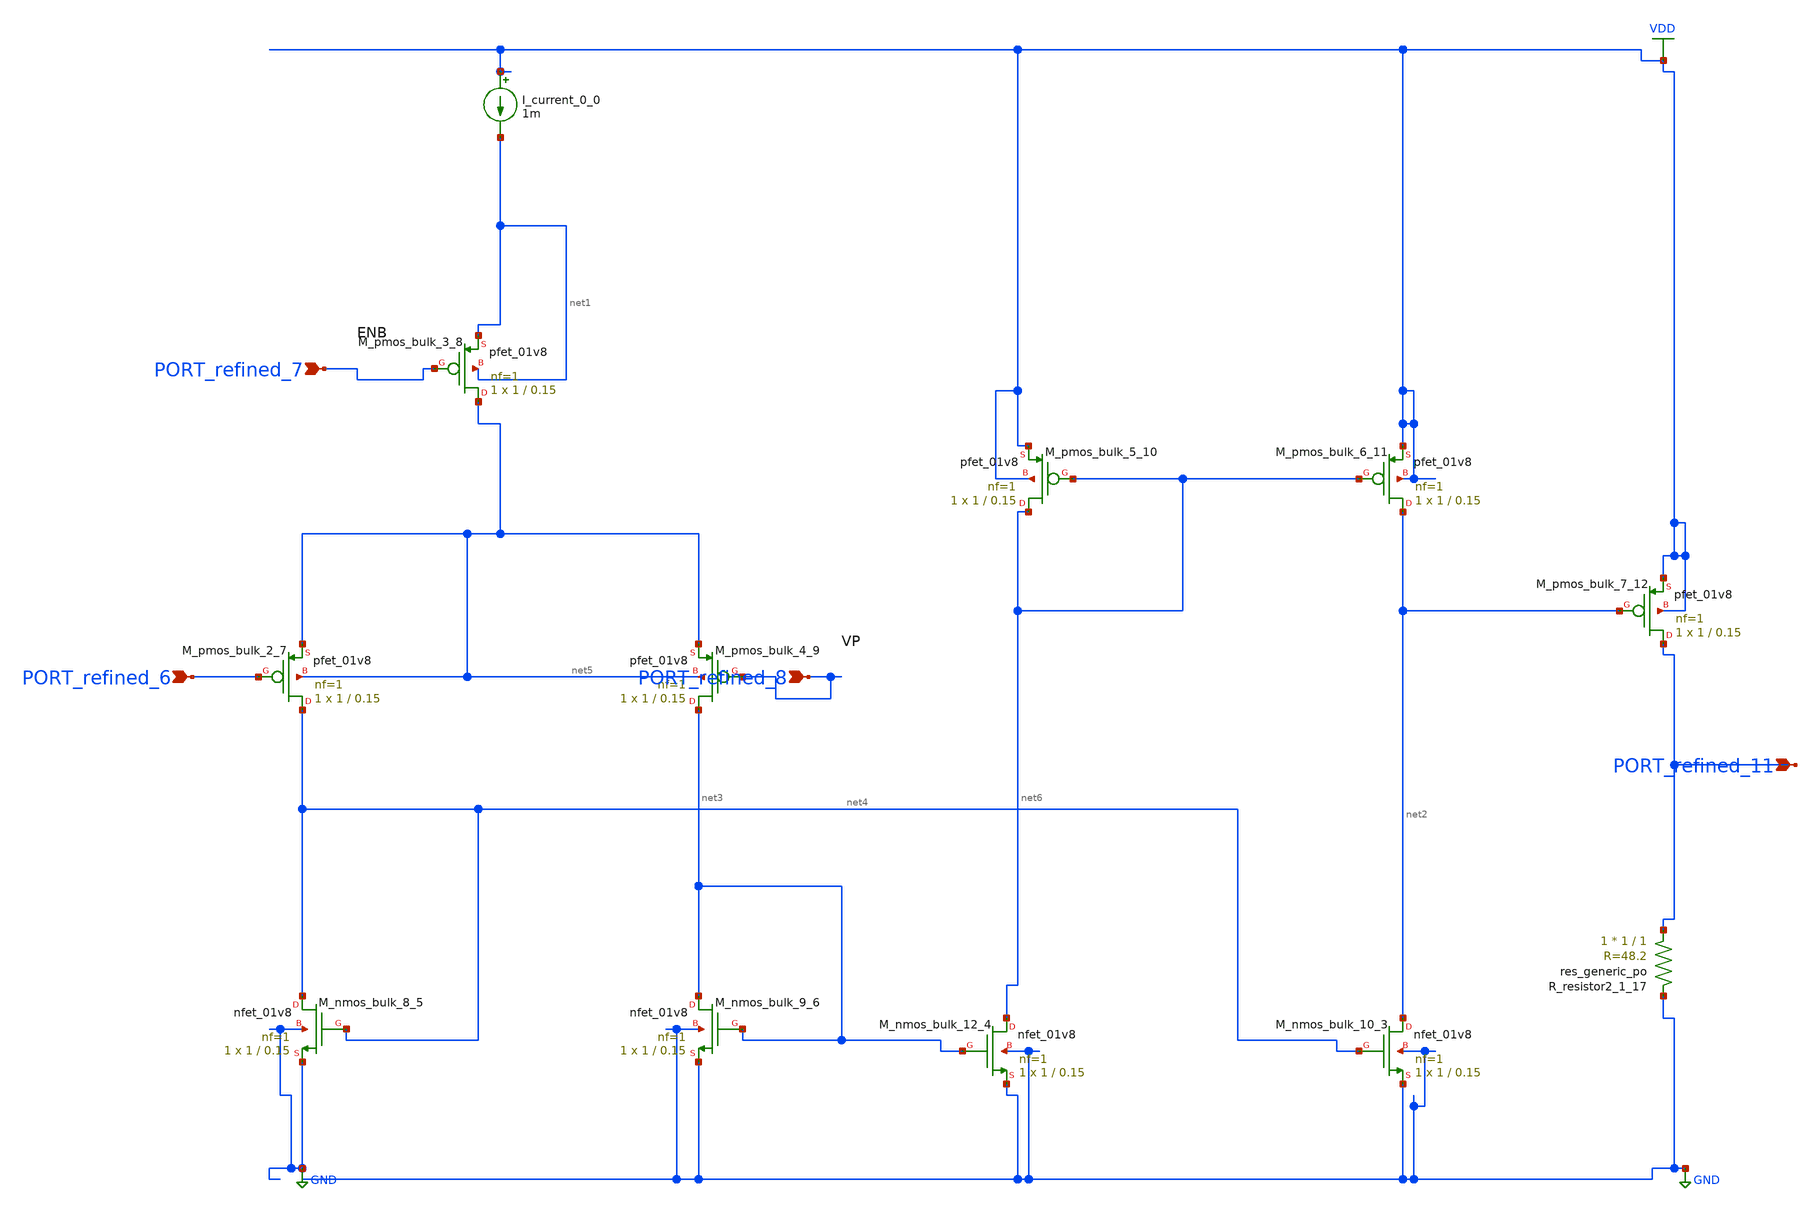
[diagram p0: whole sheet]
** sch_path: schematics/Image2Net/049.sch
**.subckt 049 PORT_refined_6 PORT_refined_11 PORT_refined_8 PORT_refined_7
*.ipin PORT_refined_6
*.ipin PORT_refined_11
*.ipin PORT_refined_8
*.ipin PORT_refined_7
I_current_0_0 VDD net1 1m
XM_nmos_bulk_10_3 net2 net4 GND GND sky130_fd_pr__nfet_01v8 L=0.15 W=1 nf=1 ad='int((1 + 1)/2) * 1 / 1 * 0.29'
+ as='int((1 + 2)/2) * 1 / 1 * 0.29' pd='2*int((1 + 1)/2) * (1 / 1 + 0.29)' ps='2*int((1 + 2)/2) * (1 / 1 + 0.29)'
+ nrd='0.29 / 1 ' nrs='0.29 / 1 ' sa=0 sb=0 sd=0 mult=1 m=1
XM_nmos_bulk_12_4 net6 net3 GND GND sky130_fd_pr__nfet_01v8 L=0.15 W=1 nf=1 ad='int((1 + 1)/2) * 1 / 1 * 0.29'
+ as='int((1 + 2)/2) * 1 / 1 * 0.29' pd='2*int((1 + 1)/2) * (1 / 1 + 0.29)' ps='2*int((1 + 2)/2) * (1 / 1 + 0.29)'
+ nrd='0.29 / 1 ' nrs='0.29 / 1 ' sa=0 sb=0 sd=0 mult=1 m=1
XM_nmos_bulk_8_5 net4 net4 GND GND sky130_fd_pr__nfet_01v8 L=0.15 W=1 nf=1 ad='int((1 + 1)/2) * 1 / 1 * 0.29'
+ as='int((1 + 2)/2) * 1 / 1 * 0.29' pd='2*int((1 + 1)/2) * (1 / 1 + 0.29)' ps='2*int((1 + 2)/2) * (1 / 1 + 0.29)'
+ nrd='0.29 / 1 ' nrs='0.29 / 1 ' sa=0 sb=0 sd=0 mult=1 m=1
XM_nmos_bulk_9_6 net3 net3 GND GND sky130_fd_pr__nfet_01v8 L=0.15 W=1 nf=1 ad='int((1 + 1)/2) * 1 / 1 * 0.29'
+ as='int((1 + 2)/2) * 1 / 1 * 0.29' pd='2*int((1 + 1)/2) * (1 / 1 + 0.29)' ps='2*int((1 + 2)/2) * (1 / 1 + 0.29)'
+ nrd='0.29 / 1 ' nrs='0.29 / 1 ' sa=0 sb=0 sd=0 mult=1 m=1
XM_pmos_bulk_2_7 net4 PORT_refined_6 net5 net5 sky130_fd_pr__pfet_01v8 L=0.15 W=1 nf=1 ad='int((1 + 1)/2) * 1 / 1 * 0.29'
+ as='int((1 + 2)/2) * 1 / 1 * 0.29' pd='2*int((1 + 1)/2) * (1 / 1 + 0.29)' ps='2*int((1 + 2)/2) * (1 / 1 + 0.29)'
+ nrd='0.29 / 1 ' nrs='0.29 / 1 ' sa=0 sb=0 sd=0 mult=1 m=1
XM_pmos_bulk_3_8 net5 PORT_refined_7 net1 net1 sky130_fd_pr__pfet_01v8 L=0.15 W=1 nf=1 ad='int((1 + 1)/2) * 1 / 1 * 0.29'
+ as='int((1 + 2)/2) * 1 / 1 * 0.29' pd='2*int((1 + 1)/2) * (1 / 1 + 0.29)' ps='2*int((1 + 2)/2) * (1 / 1 + 0.29)'
+ nrd='0.29 / 1 ' nrs='0.29 / 1 ' sa=0 sb=0 sd=0 mult=1 m=1
XM_pmos_bulk_4_9 net3 PORT_refined_8 net5 net5 sky130_fd_pr__pfet_01v8 L=0.15 W=1 nf=1 ad='int((1 + 1)/2) * 1 / 1 * 0.29'
+ as='int((1 + 2)/2) * 1 / 1 * 0.29' pd='2*int((1 + 1)/2) * (1 / 1 + 0.29)' ps='2*int((1 + 2)/2) * (1 / 1 + 0.29)'
+ nrd='0.29 / 1 ' nrs='0.29 / 1 ' sa=0 sb=0 sd=0 mult=1 m=1
XM_pmos_bulk_5_10 net6 net6 VDD VDD sky130_fd_pr__pfet_01v8 L=0.15 W=1 nf=1 ad='int((1 + 1)/2) * 1 / 1 * 0.29'
+ as='int((1 + 2)/2) * 1 / 1 * 0.29' pd='2*int((1 + 1)/2) * (1 / 1 + 0.29)' ps='2*int((1 + 2)/2) * (1 / 1 + 0.29)'
+ nrd='0.29 / 1 ' nrs='0.29 / 1 ' sa=0 sb=0 sd=0 mult=1 m=1
XM_pmos_bulk_6_11 net2 net6 VDD VDD sky130_fd_pr__pfet_01v8 L=0.15 W=1 nf=1 ad='int((1 + 1)/2) * 1 / 1 * 0.29'
+ as='int((1 + 2)/2) * 1 / 1 * 0.29' pd='2*int((1 + 1)/2) * (1 / 1 + 0.29)' ps='2*int((1 + 2)/2) * (1 / 1 + 0.29)'
+ nrd='0.29 / 1 ' nrs='0.29 / 1 ' sa=0 sb=0 sd=0 mult=1 m=1
XM_pmos_bulk_7_12 PORT_refined_11 net2 VDD VDD sky130_fd_pr__pfet_01v8 L=0.15 W=1 nf=1 ad='int((1 + 1)/2) * 1 / 1 * 0.29'
+ as='int((1 + 2)/2) * 1 / 1 * 0.29' pd='2*int((1 + 1)/2) * (1 / 1 + 0.29)' ps='2*int((1 + 2)/2) * (1 / 1 + 0.29)'
+ nrd='0.29 / 1 ' nrs='0.29 / 1 ' sa=0 sb=0 sd=0 mult=1 m=1
XR_resistor2_1_17 PORT_refined_11 GND sky130_fd_pr__res_generic_po W=1 L=1 m=1
**.ends
.GLOBAL GND
.GLOBAL VDD
.end
